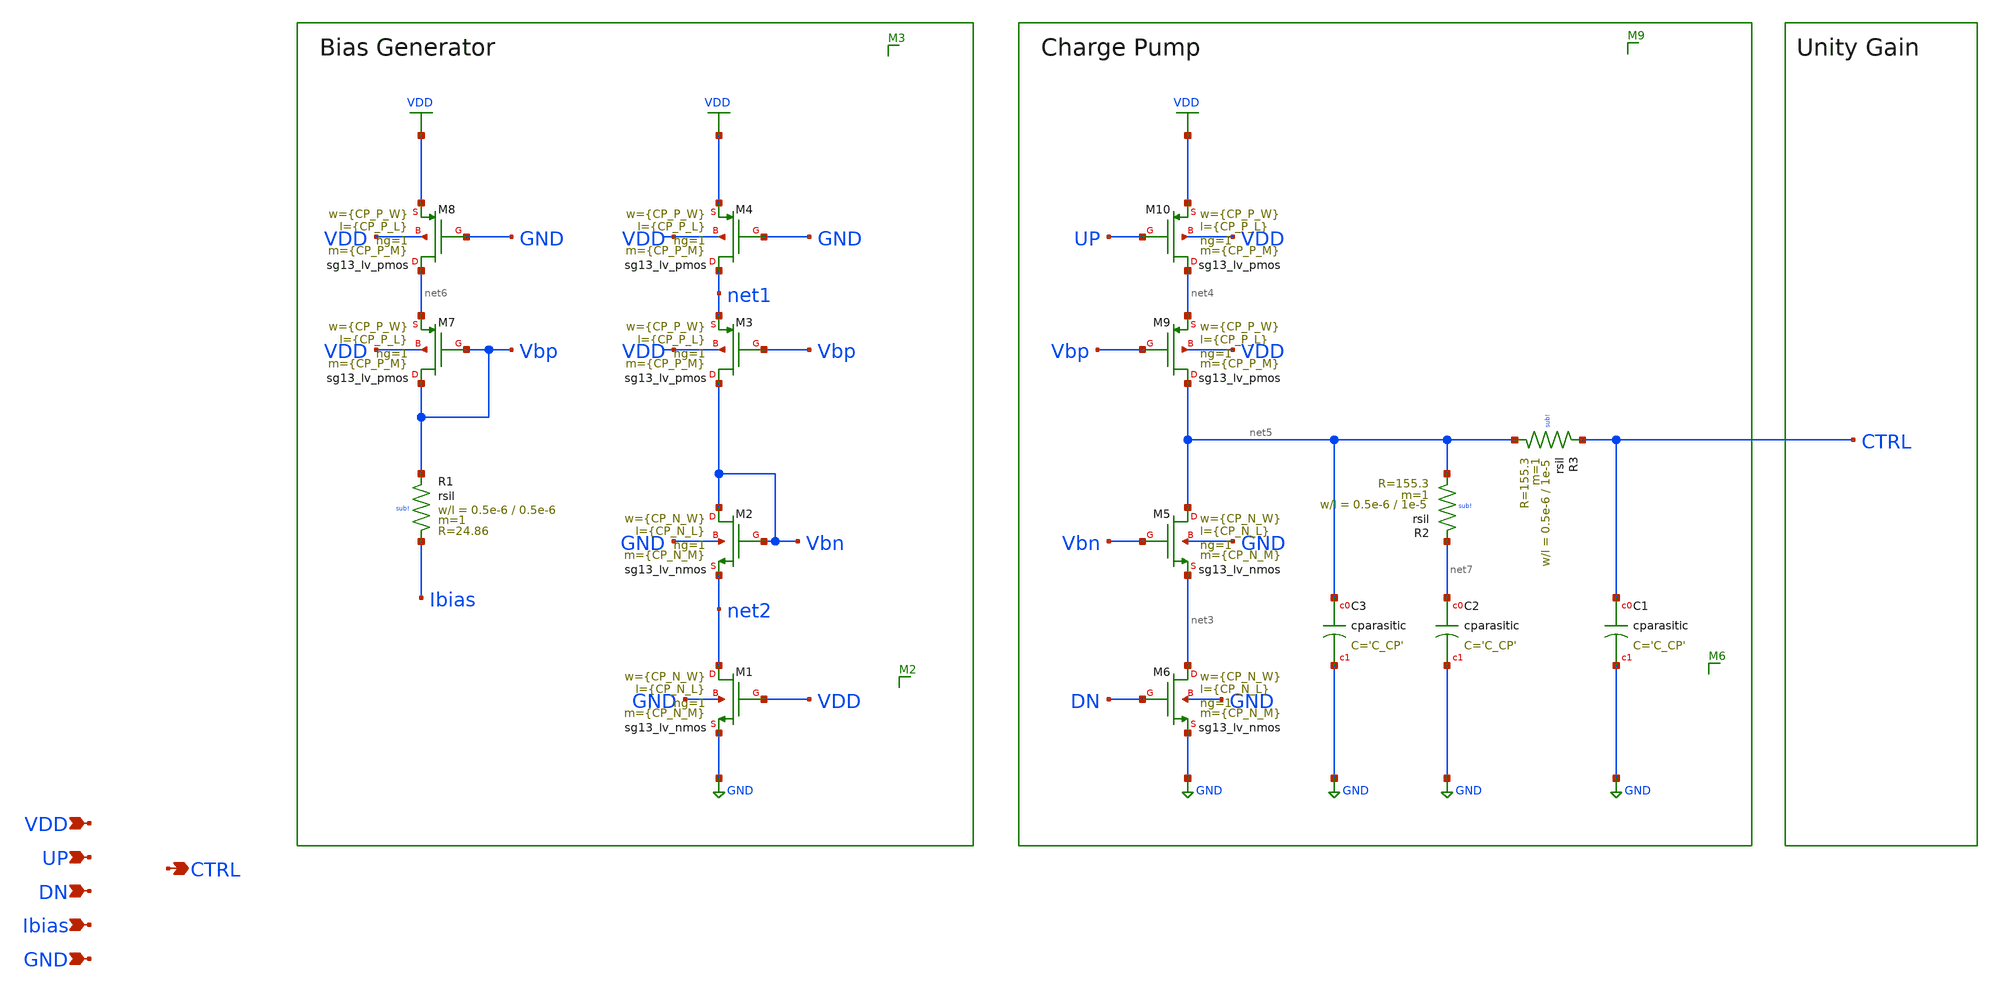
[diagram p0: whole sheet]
** sch_path: schematic/blocks/charge-pump/CP.sch
**.subckt CP CTRL UP VDD Ibias DN GND
*.opin CTRL
*.ipin UP
*.ipin VDD
*.ipin Ibias
*.ipin DN
*.ipin GND
XM2 Vbn Vbn net2 GND sg13_lv_nmos w={CP_N_W} l={CP_N_L} ng=1 m={CP_N_M} mm_ok=1
XM1 net2 VDD GND GND sg13_lv_nmos w={CP_N_W} l={CP_N_L} ng=1 m={CP_N_M} mm_ok=1
XM3 Vbn Vbp net1 VDD sg13_lv_pmos w={CP_P_W} l={CP_P_L} ng=1 m={CP_P_M} mm_ok=1
XM4 net1 GND VDD VDD sg13_lv_pmos w={CP_P_W} l={CP_P_L} ng=1 m={CP_P_M} mm_ok=1
XM7 Vbp Vbp net6 VDD sg13_lv_pmos w={CP_P_W} l={CP_P_L} ng=1 m={CP_P_M} mm_ok=1
XM8 net6 GND VDD VDD sg13_lv_pmos w={CP_P_W} l={CP_P_L} ng=1 m={CP_P_M} mm_ok=1
XM5 net5 Vbn net3 GND sg13_lv_nmos w={CP_N_W} l={CP_N_L} ng=1 m={CP_N_M} mm_ok=1
XM6 net3 DN GND GND sg13_lv_nmos w={CP_N_W} l={CP_N_L} ng=1 m={CP_N_M} mm_ok=1
XM9 net5 Vbp net4 VDD sg13_lv_pmos w={CP_P_W} l={CP_P_L} ng=1 m={CP_P_M} mm_ok=1
XM10 net4 UP VDD VDD sg13_lv_pmos w={CP_P_W} l={CP_P_L} ng=1 m={CP_P_M} mm_ok=1
XC1 CTRL GND cparasitic C='C_CP'
XR1 Vbp Ibias sub! rsil w=0.5e-6 l=0.5e-6 m=1 mm_ok=1
XR3 CTRL net5 sub! rsil w=0.5e-6 l=1e-5 m=1 mm_ok=1
XC2 net7 GND cparasitic C='C_CP'
XR2 net7 net5 sub! rsil w=0.5e-6 l=1e-5 m=1 mm_ok=1
XC3 net5 GND cparasitic C='C_CP'
**.ends
.GLOBAL GND
.GLOBAL VDD
.end
